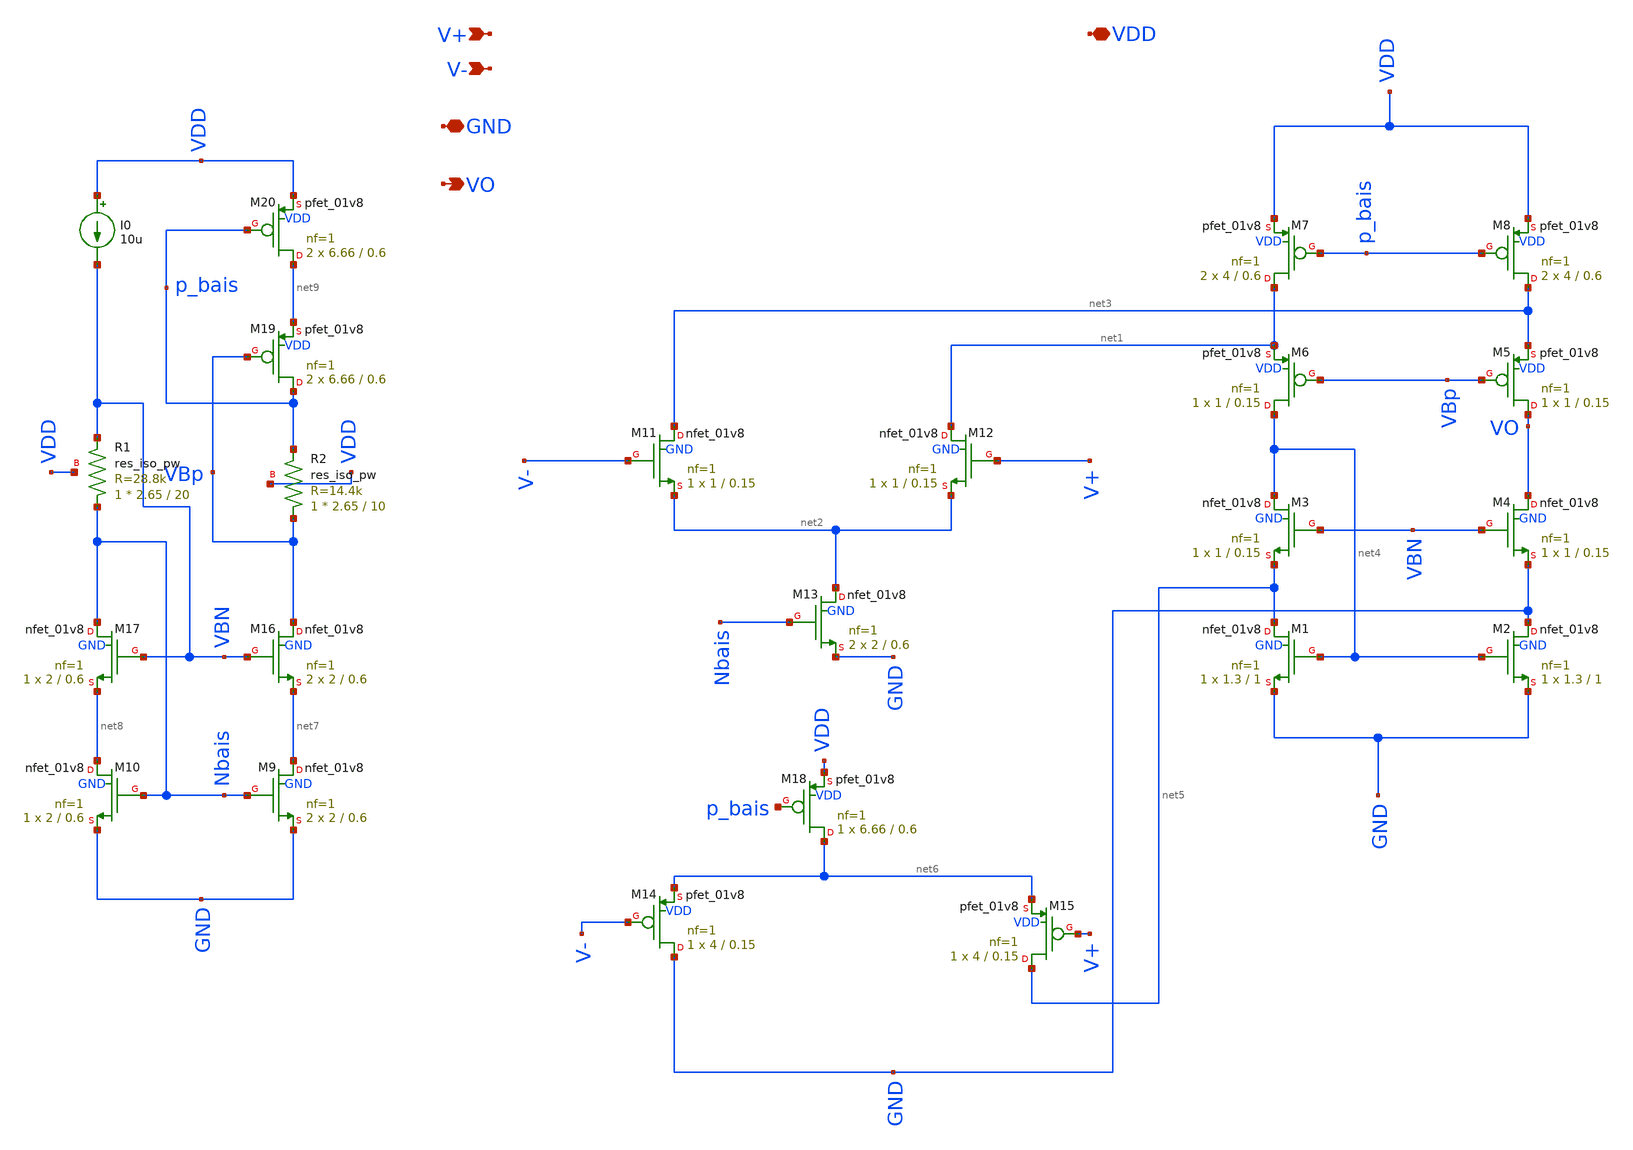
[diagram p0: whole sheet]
** sch_path: pll/pfd_cp_lf_lib/OTA/xschem/OTA.sch
**.subckt OTA VDD V+ V- VO GND
*.iopin VDD
*.ipin V+
*.ipin V-
*.opin VO
*.iopin GND
XM13 net2 Nbais GND GND sky130_fd_pr__nfet_01v8 L=0.6 W=2 nf=1 ad='int((nf+1)/2) * W/nf * 0.29' as='int((nf+2)/2) * W/nf * 0.29'
+ pd='2*int((nf+1)/2) * (W/nf + 0.29)' ps='2*int((nf+2)/2) * (W/nf + 0.29)' nrd='0.29 / W' nrs='0.29 / W'
+ sa=0 sb=0 sd=0 mult=2 m=2
XM7 net1 p_bais VDD VDD sky130_fd_pr__pfet_01v8 L=0.6 W=4 nf=1 ad='int((nf+1)/2) * W/nf * 0.29' as='int((nf+2)/2) * W/nf * 0.29'
+ pd='2*int((nf+1)/2) * (W/nf + 0.29)' ps='2*int((nf+2)/2) * (W/nf + 0.29)' nrd='0.29 / W' nrs='0.29 / W'
+ sa=0 sb=0 sd=0 mult=2 m=2
XM8 net3 p_bais VDD VDD sky130_fd_pr__pfet_01v8 L=0.6 W=4 nf=1 ad='int((nf+1)/2) * W/nf * 0.29' as='int((nf+2)/2) * W/nf * 0.29'
+ pd='2*int((nf+1)/2) * (W/nf + 0.29)' ps='2*int((nf+2)/2) * (W/nf + 0.29)' nrd='0.29 / W' nrs='0.29 / W'
+ sa=0 sb=0 sd=0 mult=2 m=2
XM11 net3 V- net2 GND sky130_fd_pr__nfet_01v8 L=0.15 W=1 nf=1 ad='int((nf+1)/2) * W/nf * 0.29' as='int((nf+2)/2) * W/nf * 0.29'
+ pd='2*int((nf+1)/2) * (W/nf + 0.29)' ps='2*int((nf+2)/2) * (W/nf + 0.29)' nrd='0.29 / W' nrs='0.29 / W'
+ sa=0 sb=0 sd=0 mult=1 m=1
XM12 net1 V+ net2 GND sky130_fd_pr__nfet_01v8 L=0.15 W=1 nf=1 ad='int((nf+1)/2) * W/nf * 0.29' as='int((nf+2)/2) * W/nf * 0.29'
+ pd='2*int((nf+1)/2) * (W/nf + 0.29)' ps='2*int((nf+2)/2) * (W/nf + 0.29)' nrd='0.29 / W' nrs='0.29 / W'
+ sa=0 sb=0 sd=0 mult=1 m=1
XM1 net5 net4 GND GND sky130_fd_pr__nfet_01v8 L=1 W=1.3 nf=1 ad='int((nf+1)/2) * W/nf * 0.29' as='int((nf+2)/2) * W/nf * 0.29'
+ pd='2*int((nf+1)/2) * (W/nf + 0.29)' ps='2*int((nf+2)/2) * (W/nf + 0.29)' nrd='0.29 / W' nrs='0.29 / W'
+ sa=0 sb=0 sd=0 mult=1 m=1
XM2 GND net4 GND GND sky130_fd_pr__nfet_01v8 L=1 W=1.3 nf=1 ad='int((nf+1)/2) * W/nf * 0.29' as='int((nf+2)/2) * W/nf * 0.29'
+ pd='2*int((nf+1)/2) * (W/nf + 0.29)' ps='2*int((nf+2)/2) * (W/nf + 0.29)' nrd='0.29 / W' nrs='0.29 / W'
+ sa=0 sb=0 sd=0 mult=1 m=1
XM3 net4 VBN net5 GND sky130_fd_pr__nfet_01v8 L=0.15 W=1 nf=1 ad='int((nf+1)/2) * W/nf * 0.29' as='int((nf+2)/2) * W/nf * 0.29'
+ pd='2*int((nf+1)/2) * (W/nf + 0.29)' ps='2*int((nf+2)/2) * (W/nf + 0.29)' nrd='0.29 / W' nrs='0.29 / W'
+ sa=0 sb=0 sd=0 mult=1 m=1
XM4 VO VBN GND GND sky130_fd_pr__nfet_01v8 L=0.15 W=1 nf=1 ad='int((nf+1)/2) * W/nf * 0.29' as='int((nf+2)/2) * W/nf * 0.29'
+ pd='2*int((nf+1)/2) * (W/nf + 0.29)' ps='2*int((nf+2)/2) * (W/nf + 0.29)' nrd='0.29 / W' nrs='0.29 / W'
+ sa=0 sb=0 sd=0 mult=1 m=1
XM5 VO VBp net3 VDD sky130_fd_pr__pfet_01v8 L=0.15 W=1 nf=1 ad='int((nf+1)/2) * W/nf * 0.29' as='int((nf+2)/2) * W/nf * 0.29'
+ pd='2*int((nf+1)/2) * (W/nf + 0.29)' ps='2*int((nf+2)/2) * (W/nf + 0.29)' nrd='0.29 / W' nrs='0.29 / W'
+ sa=0 sb=0 sd=0 mult=1 m=1
XM6 net4 VBp net1 VDD sky130_fd_pr__pfet_01v8 L=0.15 W=1 nf=1 ad='int((nf+1)/2) * W/nf * 0.29' as='int((nf+2)/2) * W/nf * 0.29'
+ pd='2*int((nf+1)/2) * (W/nf + 0.29)' ps='2*int((nf+2)/2) * (W/nf + 0.29)' nrd='0.29 / W' nrs='0.29 / W'
+ sa=0 sb=0 sd=0 mult=1 m=1
XM18 net6 p_bais VDD VDD sky130_fd_pr__pfet_01v8 L=0.6 W=6.66 nf=1 ad='int((nf+1)/2) * W/nf * 0.29' as='int((nf+2)/2) * W/nf * 0.29'
+ pd='2*int((nf+1)/2) * (W/nf + 0.29)' ps='2*int((nf+2)/2) * (W/nf + 0.29)' nrd='0.29 / W' nrs='0.29 / W'
+ sa=0 sb=0 sd=0 mult=1 m=1
XM14 GND V- net6 VDD sky130_fd_pr__pfet_01v8 L=0.15 W=4 nf=1 ad='int((nf+1)/2) * W/nf * 0.29' as='int((nf+2)/2) * W/nf * 0.29'
+ pd='2*int((nf+1)/2) * (W/nf + 0.29)' ps='2*int((nf+2)/2) * (W/nf + 0.29)' nrd='0.29 / W' nrs='0.29 / W'
+ sa=0 sb=0 sd=0 mult=1 m=1
XM15 net5 V+ net6 VDD sky130_fd_pr__pfet_01v8 L=0.15 W=4 nf=1 ad='int((nf+1)/2) * W/nf * 0.29' as='int((nf+2)/2) * W/nf * 0.29'
+ pd='2*int((nf+1)/2) * (W/nf + 0.29)' ps='2*int((nf+2)/2) * (W/nf + 0.29)' nrd='0.29 / W' nrs='0.29 / W'
+ sa=0 sb=0 sd=0 mult=1 m=1
XM9 net7 Nbais GND GND sky130_fd_pr__nfet_01v8 L=0.6 W=2 nf=1 ad='int((nf+1)/2) * W/nf * 0.29' as='int((nf+2)/2) * W/nf * 0.29'
+ pd='2*int((nf+1)/2) * (W/nf + 0.29)' ps='2*int((nf+2)/2) * (W/nf + 0.29)' nrd='0.29 / W' nrs='0.29 / W'
+ sa=0 sb=0 sd=0 mult=2 m=2
XM10 net8 Nbais GND GND sky130_fd_pr__nfet_01v8 L=0.6 W=2 nf=1 ad='int((nf+1)/2) * W/nf * 0.29' as='int((nf+2)/2) * W/nf * 0.29'
+ pd='2*int((nf+1)/2) * (W/nf + 0.29)' ps='2*int((nf+2)/2) * (W/nf + 0.29)' nrd='0.29 / W' nrs='0.29 / W'
+ sa=0 sb=0 sd=0 mult=1 m=1
XM16 VBp VBN net7 GND sky130_fd_pr__nfet_01v8 L=0.6 W=2 nf=1 ad='int((nf+1)/2) * W/nf * 0.29' as='int((nf+2)/2) * W/nf * 0.29'
+ pd='2*int((nf+1)/2) * (W/nf + 0.29)' ps='2*int((nf+2)/2) * (W/nf + 0.29)' nrd='0.29 / W' nrs='0.29 / W'
+ sa=0 sb=0 sd=0 mult=2 m=2
XM17 Nbais VBN net8 GND sky130_fd_pr__nfet_01v8 L=0.6 W=2 nf=1 ad='int((nf+1)/2) * W/nf * 0.29' as='int((nf+2)/2) * W/nf * 0.29'
+ pd='2*int((nf+1)/2) * (W/nf + 0.29)' ps='2*int((nf+2)/2) * (W/nf + 0.29)' nrd='0.29 / W' nrs='0.29 / W'
+ sa=0 sb=0 sd=0 mult=1 m=1
XM19 p_bais VBp net9 VDD sky130_fd_pr__pfet_01v8 L=0.6 W=6.66 nf=1 ad='int((nf+1)/2) * W/nf * 0.29' as='int((nf+2)/2) * W/nf * 0.29'
+ pd='2*int((nf+1)/2) * (W/nf + 0.29)' ps='2*int((nf+2)/2) * (W/nf + 0.29)' nrd='0.29 / W' nrs='0.29 / W'
+ sa=0 sb=0 sd=0 mult=2 m=2
XM20 net9 p_bais VDD VDD sky130_fd_pr__pfet_01v8 L=0.6 W=6.66 nf=1 ad='int((nf+1)/2) * W/nf * 0.29' as='int((nf+2)/2) * W/nf * 0.29'
+ pd='2*int((nf+1)/2) * (W/nf + 0.29)' ps='2*int((nf+2)/2) * (W/nf + 0.29)' nrd='0.29 / W' nrs='0.29 / W'
+ sa=0 sb=0 sd=0 mult=2 m=2
I0 VDD VBN 10u
XR1 Nbais VBN VDD sky130_fd_pr__res_iso_pw W=2.65 L=20 m=1
XR2 VBp p_bais VDD sky130_fd_pr__res_iso_pw W=2.65 L=10 m=1
**.ends
.end
